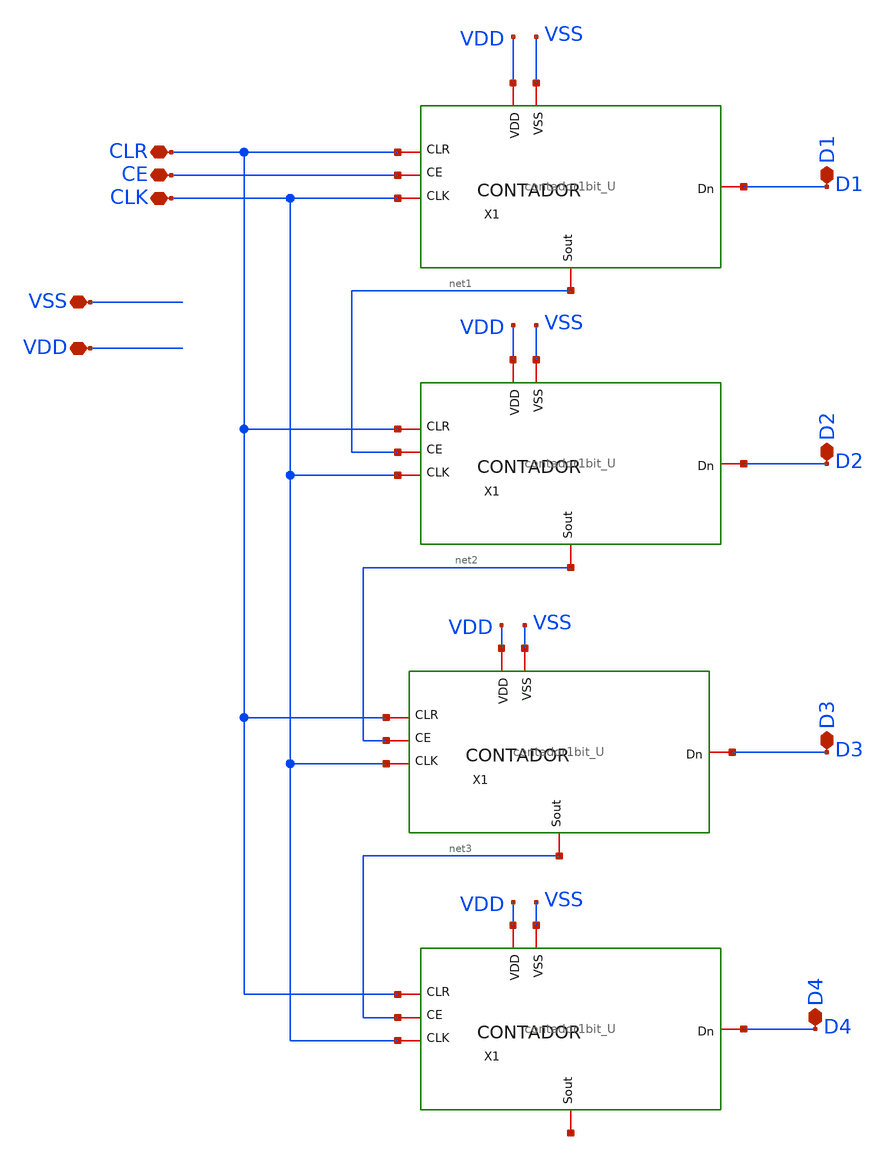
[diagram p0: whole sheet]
** sch_path: design/blocks/contador4bits_U/schematic/Contador4bits_U.sch
**.subckt Contador4bits_U CLR CE CLK VDD VSS D1 D2 D3 D4
*.iopin CLR
*.iopin CE
*.iopin CLK
*.iopin VDD
*.iopin VSS
*.iopin D1
*.iopin D2
*.iopin D3
*.iopin D4
x1 VDD VSS net1 CLR D2 CLK net2 contador1bit_U
x2 VDD VSS net2 CLR D3 CLK net3 contador1bit_U
x3 VDD VSS net3 CLR D4 CLK net4 contador1bit_U
x4 VDD VSS CE CLR D1 CLK net1 contador1bit_U
**.ends
.end
